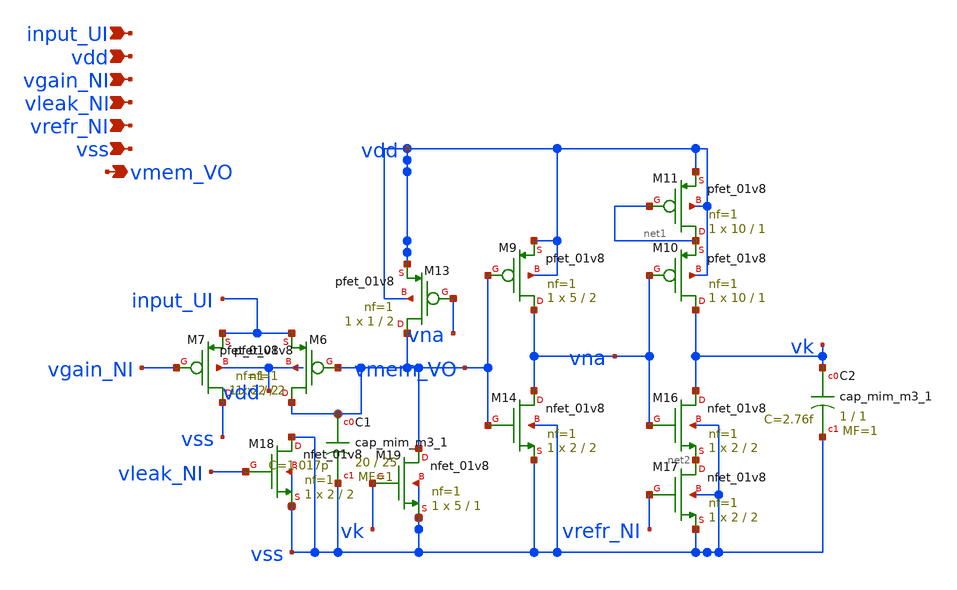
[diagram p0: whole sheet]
** sch_path: circuits/DPI_neuron.sch
* Copyright 2020 Stefan Frederik Schippers
* Licensed under the Apache License, Version 2.0 (the "License");
* you may not use this file except in compliance with the License.
* You may obtain a copy of the License at
* https://www.apache.org/licenses/LICENSE-2.0
* Unless required by applicable law or agreed to in writing, software
* distributed under the License is distributed on an "AS IS" BASIS,
* WITHOUT WARRANTIES OR CONDITIONS OF ANY KIND, either express or implied.
* See the License for the specific language governing permissions and
* limitations under the License.
**.subckt DPI_neuron vdd vgain_NI vleak_NI vrefr_NI vss input_UI vmem_VO
*.ipin vdd
*.ipin vgain_NI
*.ipin vleak_NI
*.ipin vrefr_NI
*.ipin vss
*.ipin input_UI
*.opin vmem_VO
XM6 vmem_VO vmem_VO input_UI vdd sky130_fd_pr__pfet_01v8 L=2 W=2 nf=1 ad='int((nf+1)/2) * W/nf * 0.29'
+ as='int((nf+2)/2) * W/nf * 0.29' pd='2*int((nf+1)/2) * (W/nf + 0.29)' ps='2*int((nf+2)/2) * (W/nf + 0.29)'
+ nrd='0.29 / W' nrs='0.29 / W' sa=0 sb=0 sd=0 mult=1 m=1
XM7 vss vgain_NI input_UI vdd sky130_fd_pr__pfet_01v8 L=2 W=2 nf=1 ad='int((nf+1)/2) * W/nf * 0.29' as='int((nf+2)/2) * W/nf * 0.29'
+ pd='2*int((nf+1)/2) * (W/nf + 0.29)' ps='2*int((nf+2)/2) * (W/nf + 0.29)' nrd='0.29 / W' nrs='0.29 / W'
+ sa=0 sb=0 sd=0 mult=1 m=1
XM9 vna vmem_VO vdd vdd sky130_fd_pr__pfet_01v8 L=2 W=5 nf=1 ad='int((nf+1)/2) * W/nf * 0.29' as='int((nf+2)/2) * W/nf * 0.29'
+ pd='2*int((nf+1)/2) * (W/nf + 0.29)' ps='2*int((nf+2)/2) * (W/nf + 0.29)' nrd='0.29 / W' nrs='0.29 / W'
+ sa=0 sb=0 sd=0 mult=1 m=1
XM10 vk vna net1 vdd sky130_fd_pr__pfet_01v8 L=1 W=10 nf=1 ad='int((nf+1)/2) * W/nf * 0.29' as='int((nf+2)/2) * W/nf * 0.29'
+ pd='2*int((nf+1)/2) * (W/nf + 0.29)' ps='2*int((nf+2)/2) * (W/nf + 0.29)' nrd='0.29 / W' nrs='0.29 / W'
+ sa=0 sb=0 sd=0 mult=1 m=1
XM11 net1 net1 vdd vdd sky130_fd_pr__pfet_01v8 L=1 W=10 nf=1 ad='int((nf+1)/2) * W/nf * 0.29' as='int((nf+2)/2) * W/nf * 0.29'
+ pd='2*int((nf+1)/2) * (W/nf + 0.29)' ps='2*int((nf+2)/2) * (W/nf + 0.29)' nrd='0.29 / W' nrs='0.29 / W'
+ sa=0 sb=0 sd=0 mult=1 m=1
XM13 vmem_VO vna vdd vdd sky130_fd_pr__pfet_01v8 L=2 W=1 nf=1 ad='int((nf+1)/2) * W/nf * 0.29' as='int((nf+2)/2) * W/nf * 0.29'
+ pd='2*int((nf+1)/2) * (W/nf + 0.29)' ps='2*int((nf+2)/2) * (W/nf + 0.29)' nrd='0.29 / W' nrs='0.29 / W'
+ sa=0 sb=0 sd=0 mult=1 m=1
XM14 vna vmem_VO vss vss sky130_fd_pr__nfet_01v8 L=2 W=2 nf=1 ad='int((nf+1)/2) * W/nf * 0.29' as='int((nf+2)/2) * W/nf * 0.29'
+ pd='2*int((nf+1)/2) * (W/nf + 0.29)' ps='2*int((nf+2)/2) * (W/nf + 0.29)' nrd='0.29 / W' nrs='0.29 / W'
+ sa=0 sb=0 sd=0 mult=1 m=1
XM16 vk vna net2 vss sky130_fd_pr__nfet_01v8 L=2 W=2 nf=1 ad='int((nf+1)/2) * W/nf * 0.29' as='int((nf+2)/2) * W/nf * 0.29'
+ pd='2*int((nf+1)/2) * (W/nf + 0.29)' ps='2*int((nf+2)/2) * (W/nf + 0.29)' nrd='0.29 / W' nrs='0.29 / W'
+ sa=0 sb=0 sd=0 mult=1 m=1
XM17 net2 vrefr_NI vss vss sky130_fd_pr__nfet_01v8 L=2 W=2 nf=1 ad='int((nf+1)/2) * W/nf * 0.29' as='int((nf+2)/2) * W/nf * 0.29'
+ pd='2*int((nf+1)/2) * (W/nf + 0.29)' ps='2*int((nf+2)/2) * (W/nf + 0.29)' nrd='0.29 / W' nrs='0.29 / W'
+ sa=0 sb=0 sd=0 mult=1 m=1
XM18 vss vleak_NI vss vss sky130_fd_pr__nfet_01v8 L=2 W=2 nf=1 ad='int((nf+1)/2) * W/nf * 0.29' as='int((nf+2)/2) * W/nf * 0.29'
+ pd='2*int((nf+1)/2) * (W/nf + 0.29)' ps='2*int((nf+2)/2) * (W/nf + 0.29)' nrd='0.29 / W' nrs='0.29 / W'
+ sa=0 sb=0 sd=0 mult=1 m=1
XM19 vmem_VO vk vss vss sky130_fd_pr__nfet_01v8 L=1 W=5 nf=1 ad='int((nf+1)/2) * W/nf * 0.29' as='int((nf+2)/2) * W/nf * 0.29'
+ pd='2*int((nf+1)/2) * (W/nf + 0.29)' ps='2*int((nf+2)/2) * (W/nf + 0.29)' nrd='0.29 / W' nrs='0.29 / W'
+ sa=0 sb=0 sd=0 mult=1 m=1
XC1 vmem_VO vss sky130_fd_pr__cap_mim_m3_1 W=20 L=25 MF=1 m=1
XC2 vk vss sky130_fd_pr__cap_mim_m3_1 W=1 L=1 MF=1 m=1
**** begin user architecture code
 .lib $::SKYWATER_MODELS/models/sky130.lib.spice tt

.param mc_mm_switch=0
.param mc_pr_switch=1


**** end user architecture code
**.ends
.end
